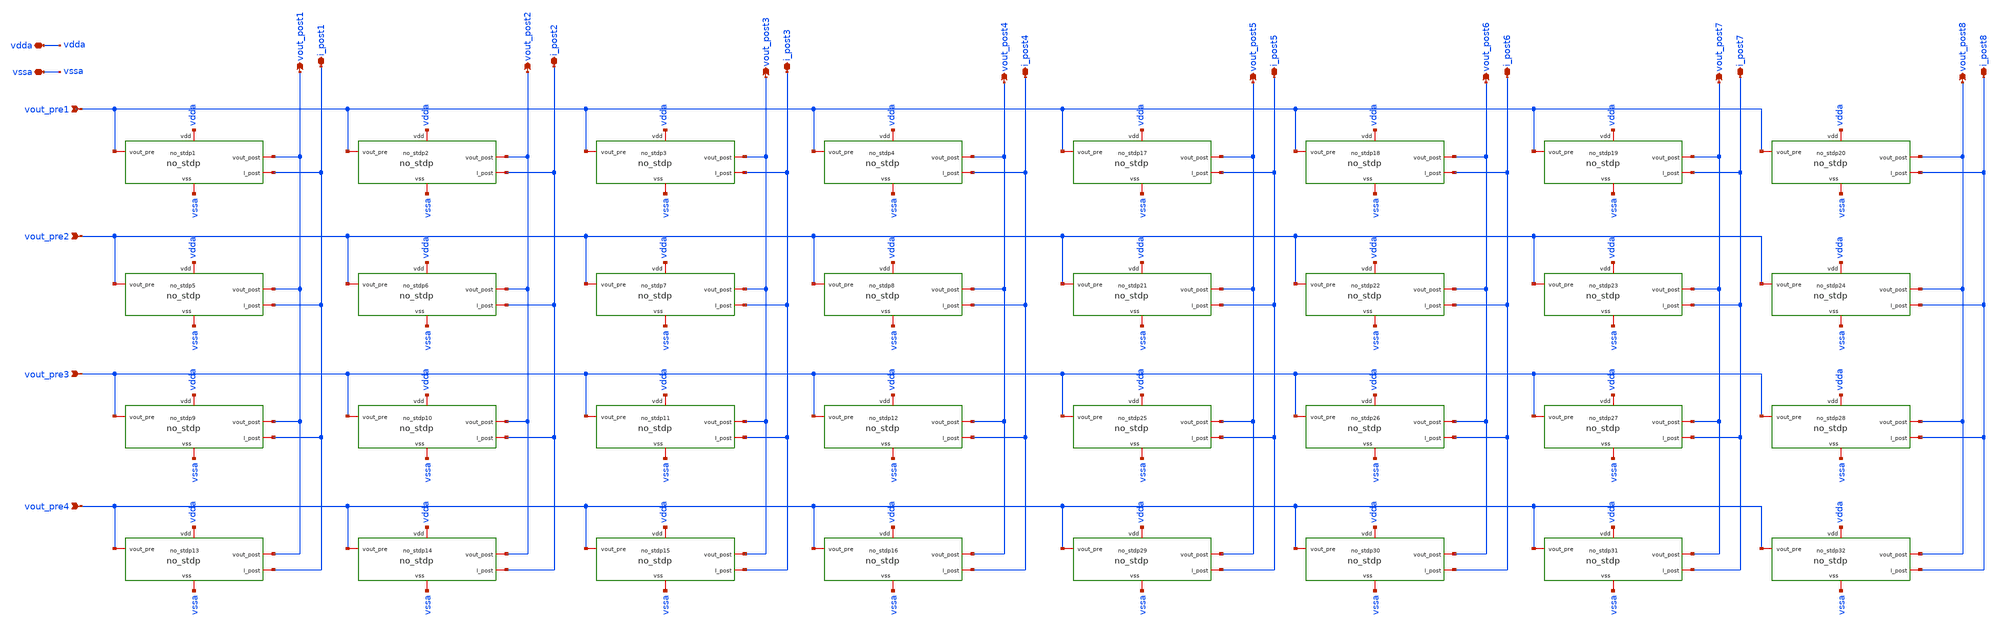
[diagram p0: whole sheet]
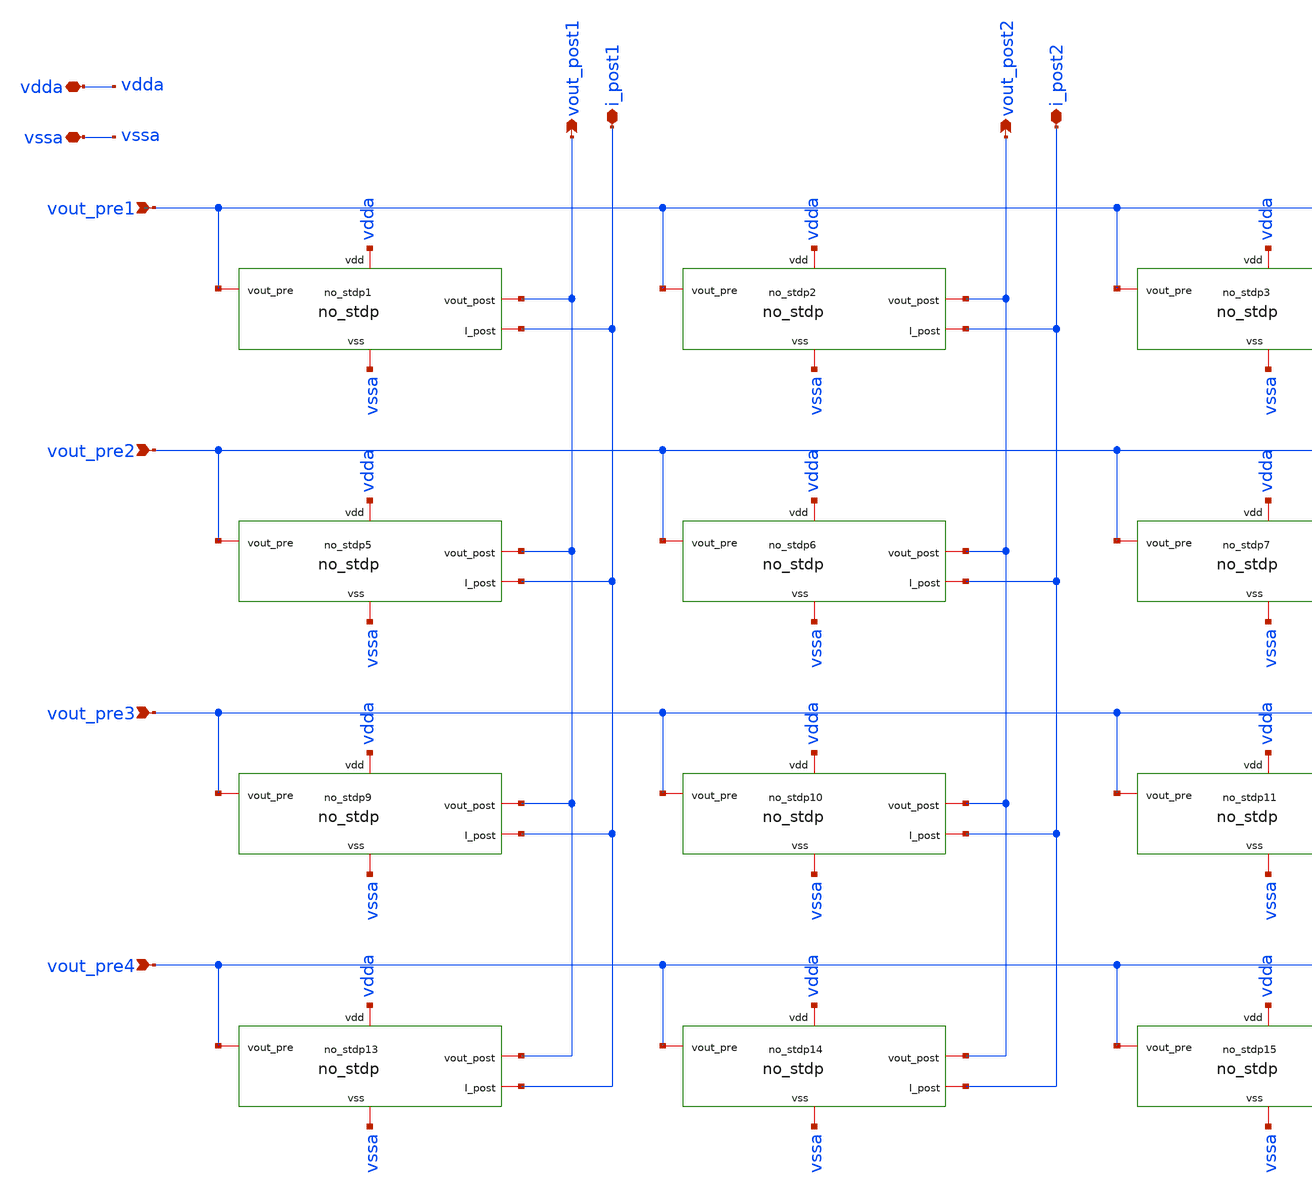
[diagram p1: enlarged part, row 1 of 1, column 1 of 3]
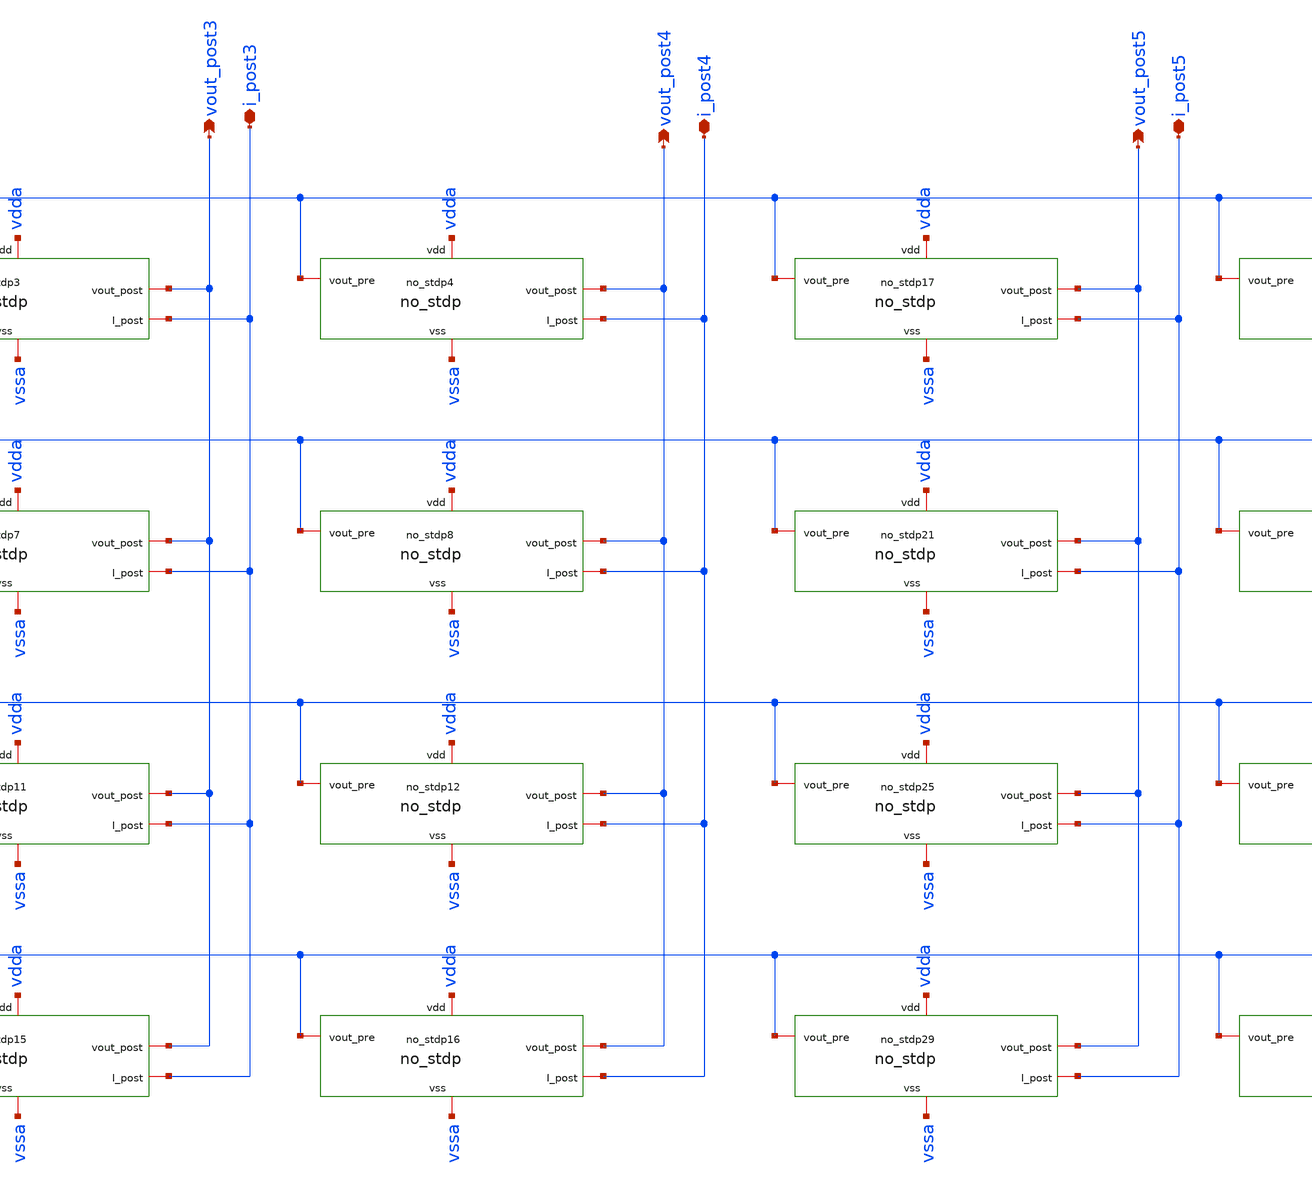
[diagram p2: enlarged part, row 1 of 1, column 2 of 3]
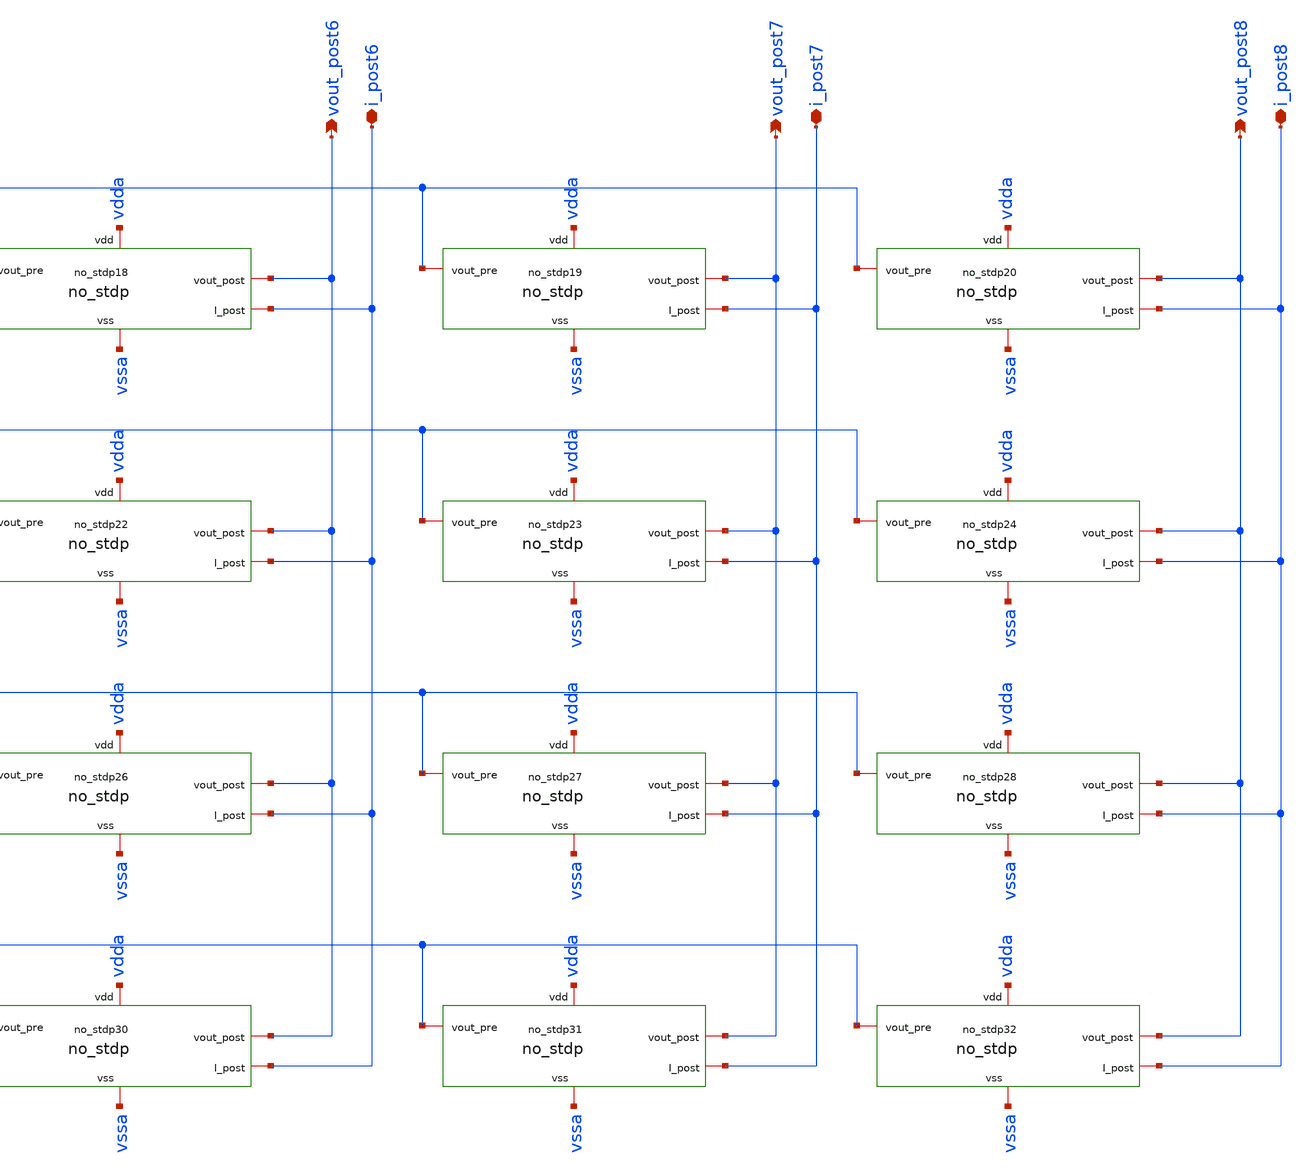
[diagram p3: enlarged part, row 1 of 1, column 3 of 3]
** sch_path: Synapse/no_stdp_4x8.sch
**.subckt no_stdp_4x8 vout_pre1 vout_post1 vdda vssa i_post1 i_post3 i_post4 vout_pre2 vout_pre3
*+ vout_pre4 vout_post2 vout_post3 vout_post4 i_post2 i_post5 vout_post5 i_post6 vout_post6 i_post7 vout_post7
*+ i_post8 vout_post8
*.ipin vout_pre1
*.opin vout_post1
*.iopin vdda
*.iopin vssa
*.iopin i_post1
*.iopin i_post3
*.iopin i_post4
*.ipin vout_pre2
*.ipin vout_pre3
*.ipin vout_pre4
*.opin vout_post2
*.opin vout_post3
*.opin vout_post4
*.iopin i_post2
*.iopin i_post5
*.opin vout_post5
*.iopin i_post6
*.opin vout_post6
*.iopin i_post7
*.opin vout_post7
*.iopin i_post8
*.opin vout_post8
xno_stdp1 vdda vssa vout_pre1 vout_post1 i_post1 no_stdp
xno_stdp2 vdda vssa vout_pre1 vout_post2 i_post2 no_stdp
xno_stdp3 vdda vssa vout_pre1 vout_post3 i_post3 no_stdp
xno_stdp4 vdda vssa vout_pre1 vout_post4 i_post4 no_stdp
xno_stdp5 vdda vssa vout_pre2 vout_post1 i_post1 no_stdp
xno_stdp6 vdda vssa vout_pre2 vout_post2 i_post2 no_stdp
xno_stdp7 vdda vssa vout_pre2 vout_post3 i_post3 no_stdp
xno_stdp8 vdda vssa vout_pre2 vout_post4 i_post4 no_stdp
xno_stdp9 vdda vssa vout_pre3 vout_post1 i_post1 no_stdp
xno_stdp10 vdda vssa vout_pre3 vout_post2 i_post2 no_stdp
xno_stdp11 vdda vssa vout_pre3 vout_post3 i_post3 no_stdp
xno_stdp12 vdda vssa vout_pre3 vout_post4 i_post4 no_stdp
xno_stdp13 vdda vssa vout_pre4 vout_post1 i_post1 no_stdp
xno_stdp14 vdda vssa vout_pre4 vout_post2 i_post2 no_stdp
xno_stdp15 vdda vssa vout_pre4 vout_post3 i_post3 no_stdp
xno_stdp16 vdda vssa vout_pre4 vout_post4 i_post4 no_stdp
xno_stdp17 vdda vssa vout_pre1 vout_post5 i_post5 no_stdp
xno_stdp18 vdda vssa vout_pre1 vout_post6 i_post6 no_stdp
xno_stdp19 vdda vssa vout_pre1 vout_post7 i_post7 no_stdp
xno_stdp20 vdda vssa vout_pre1 vout_post8 i_post8 no_stdp
xno_stdp21 vdda vssa vout_pre2 vout_post5 i_post5 no_stdp
xno_stdp22 vdda vssa vout_pre2 vout_post6 i_post6 no_stdp
xno_stdp23 vdda vssa vout_pre2 vout_post7 i_post7 no_stdp
xno_stdp24 vdda vssa vout_pre2 vout_post8 i_post8 no_stdp
xno_stdp25 vdda vssa vout_pre3 vout_post5 i_post5 no_stdp
xno_stdp26 vdda vssa vout_pre3 vout_post6 i_post6 no_stdp
xno_stdp27 vdda vssa vout_pre3 vout_post7 i_post7 no_stdp
xno_stdp28 vdda vssa vout_pre3 vout_post8 i_post8 no_stdp
xno_stdp29 vdda vssa vout_pre4 vout_post5 i_post5 no_stdp
xno_stdp30 vdda vssa vout_pre4 vout_post6 i_post6 no_stdp
xno_stdp31 vdda vssa vout_pre4 vout_post7 i_post7 no_stdp
xno_stdp32 vdda vssa vout_pre4 vout_post8 i_post8 no_stdp
**.ends

* expanding   symbol:  Synapse/no_stdp.sym # of pins=5
** sym_path: Synapse/no_stdp.sym
** sch_path: Synapse/no_stdp.sch
.subckt no_stdp vdd vss vout_pre vout_post I_post
*.iopin vdd
*.iopin vss
*.iopin vout_post
*.iopin vout_pre
*.iopin I_post
XM3 be vout_post vss vss sky130_fd_pr__nfet_01v8 L=0.15 W=5 nf=1 ad='int((nf+1)/2) * W/nf * 0.29' as='int((nf+2)/2) * W/nf * 0.29'
+ pd='2*int((nf+1)/2) * (W/nf + 0.29)' ps='2*int((nf+2)/2) * (W/nf + 0.29)' nrd='0.29 / W' nrs='0.29 / W'
+ sa=0 sb=0 sd=0 mult=1 m=1
XM4 net1 vout_pre vss vss sky130_fd_pr__nfet_01v8 L=0.15 W=5 nf=1 ad='int((nf+1)/2) * W/nf * 0.29' as='int((nf+2)/2) * W/nf * 0.29'
+ pd='2*int((nf+1)/2) * (W/nf + 0.29)' ps='2*int((nf+2)/2) * (W/nf + 0.29)' nrd='0.29 / W' nrs='0.29 / W'
+ sa=0 sb=0 sd=0 mult=1 m=1
XM14 net3 net2 vdd vdd sky130_fd_pr__pfet_01v8 L=5 W=0.75 nf=1 ad='int((nf+1)/2) * W/nf * 0.29' as='int((nf+2)/2) * W/nf * 0.29'
+ pd='2*int((nf+1)/2) * (W/nf + 0.29)' ps='2*int((nf+2)/2) * (W/nf + 0.29)' nrd='0.29 / W' nrs='0.29 / W'
+ sa=0 sb=0 sd=0 mult=1 m=1
XM15 net2 net2 vdd vdd sky130_fd_pr__pfet_01v8 L=0.15 W=10 nf=1 ad='int((nf+1)/2) * W/nf * 0.29' as='int((nf+2)/2) * W/nf * 0.29'
+ pd='2*int((nf+1)/2) * (W/nf + 0.29)' ps='2*int((nf+2)/2) * (W/nf + 0.29)' nrd='0.29 / W' nrs='0.29 / W'
+ sa=0 sb=0 sd=0 mult=1 m=1
**** begin user architecture code


.save v(te) v(be) i(vmr)


**** end user architecture code
Vmr te net1 0
.save i(vmr)
XM5 n_vout_pre vout_pre vdd vdd sky130_fd_pr__pfet_01v8 L=0.15 W=1 nf=1 ad='int((nf+1)/2) * W/nf * 0.29'
+ as='int((nf+2)/2) * W/nf * 0.29' pd='2*int((nf+1)/2) * (W/nf + 0.29)' ps='2*int((nf+2)/2) * (W/nf + 0.29)'
+ nrd='0.29 / W' nrs='0.29 / W' sa=0 sb=0 sd=0 mult=1 m=1
XM7 n_vout_pre vout_pre vss vss sky130_fd_pr__nfet_01v8 L=0.15 W=1 nf=1 ad='int((nf+1)/2) * W/nf * 0.29'
+ as='int((nf+2)/2) * W/nf * 0.29' pd='2*int((nf+1)/2) * (W/nf + 0.29)' ps='2*int((nf+2)/2) * (W/nf + 0.29)'
+ nrd='0.29 / W' nrs='0.29 / W' sa=0 sb=0 sd=0 mult=1 m=1
XM8 n_vout_post vout_post vdd vdd sky130_fd_pr__pfet_01v8 L=0.15 W=1 nf=1 ad='int((nf+1)/2) * W/nf * 0.29'
+ as='int((nf+2)/2) * W/nf * 0.29' pd='2*int((nf+1)/2) * (W/nf + 0.29)' ps='2*int((nf+2)/2) * (W/nf + 0.29)'
+ nrd='0.29 / W' nrs='0.29 / W' sa=0 sb=0 sd=0 mult=1 m=1
XM9 n_vout_post vout_post vss vss sky130_fd_pr__nfet_01v8 L=0.15 W=1 nf=1 ad='int((nf+1)/2) * W/nf * 0.29'
+ as='int((nf+2)/2) * W/nf * 0.29' pd='2*int((nf+1)/2) * (W/nf + 0.29)' ps='2*int((nf+2)/2) * (W/nf + 0.29)'
+ nrd='0.29 / W' nrs='0.29 / W' sa=0 sb=0 sd=0 mult=1 m=1
XM1 net1 n_vout_post net2 vss sky130_fd_pr__pfet_01v8 L=0.15 W=10 nf=1 ad='int((nf+1)/2) * W/nf * 0.29'
+ as='int((nf+2)/2) * W/nf * 0.29' pd='2*int((nf+1)/2) * (W/nf + 0.29)' ps='2*int((nf+2)/2) * (W/nf + 0.29)'
+ nrd='0.29 / W' nrs='0.29 / W' sa=0 sb=0 sd=0 mult=1 m=1
XM2 be n_vout_pre net2 vss sky130_fd_pr__pfet_01v8 L=0.15 W=10 nf=1 ad='int((nf+1)/2) * W/nf * 0.29'
+ as='int((nf+2)/2) * W/nf * 0.29' pd='2*int((nf+1)/2) * (W/nf + 0.29)' ps='2*int((nf+2)/2) * (W/nf + 0.29)'
+ nrd='0.29 / W' nrs='0.29 / W' sa=0 sb=0 sd=0 mult=1 m=1
XM6 I_post net2 net3 vdd sky130_fd_pr__pfet_01v8 L=5 W=0.75 nf=1 ad='int((nf+1)/2) * W/nf * 0.29' as='int((nf+2)/2) * W/nf * 0.29'
+ pd='2*int((nf+1)/2) * (W/nf + 0.29)' ps='2*int((nf+2)/2) * (W/nf + 0.29)' nrd='0.29 / W' nrs='0.29 / W'
+ sa=0 sb=0 sd=0 mult=1 m=1
R1 be te 'AGAUSS((3300000)/2,500000, 1)' m=1
.ends

.end
